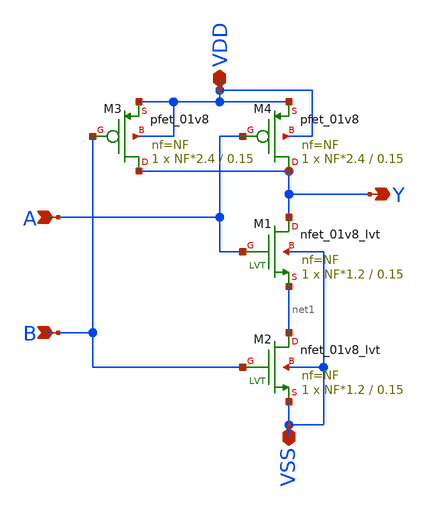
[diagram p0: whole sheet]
** sch_path: xschem_lib/DFFRAM_full_custom/nand.sch
**.subckt nand Y A VDD VSS B
*.opin Y
*.ipin A
*.iopin VDD
*.iopin VSS
*.ipin B
XM1 Y A net1 VSS sky130_fd_pr__nfet_01v8_lvt L=0.15 W=NF*1.2 nf=NF ad='int((nf+1)/2) * W/nf * 0.29' as='int((nf+2)/2) * W/nf * 0.29'
+ pd='2*int((nf+1)/2) * (W/nf + 0.29)' ps='2*int((nf+2)/2) * (W/nf + 0.29)' nrd='0.29 / W' nrs='0.29 / W'
+ sa=0 sb=0 sd=0 mult=1 m=1
XM3 Y B VDD VDD sky130_fd_pr__pfet_01v8 L=0.15 W=NF*2.4 nf=NF ad='int((nf+1)/2) * W/nf * 0.29' as='int((nf+2)/2) * W/nf * 0.29'
+ pd='2*int((nf+1)/2) * (W/nf + 0.29)' ps='2*int((nf+2)/2) * (W/nf + 0.29)' nrd='0.29 / W' nrs='0.29 / W'
+ sa=0 sb=0 sd=0 mult=1 m=1
XM4 Y A VDD VDD sky130_fd_pr__pfet_01v8 L=0.15 W=NF*2.4 nf=NF ad='int((nf+1)/2) * W/nf * 0.29' as='int((nf+2)/2) * W/nf * 0.29'
+ pd='2*int((nf+1)/2) * (W/nf + 0.29)' ps='2*int((nf+2)/2) * (W/nf + 0.29)' nrd='0.29 / W' nrs='0.29 / W'
+ sa=0 sb=0 sd=0 mult=1 m=1
XM2 net1 B VSS VSS sky130_fd_pr__nfet_01v8_lvt L=0.15 W=NF*1.2 nf=NF ad='int((nf+1)/2) * W/nf * 0.29'
+ as='int((nf+2)/2) * W/nf * 0.29' pd='2*int((nf+1)/2) * (W/nf + 0.29)' ps='2*int((nf+2)/2) * (W/nf + 0.29)'
+ nrd='0.29 / W' nrs='0.29 / W' sa=0 sb=0 sd=0 mult=1 m=1
**.ends
.end
